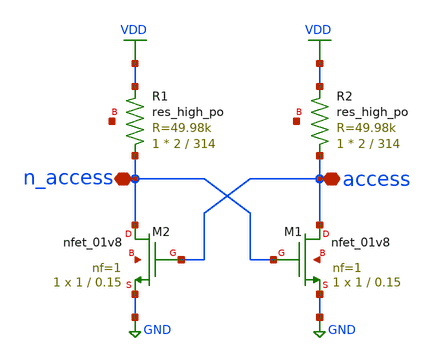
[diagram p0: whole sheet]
** sch_path: analog/schematics/2T2R.sch
**.subckt 2T2R access n_access
*.iopin access
*.iopin n_access
XM1 access n_access GND net1 sky130_fd_pr__nfet_01v8 L=0.15 W=1 nf=1 ad='int((nf+1)/2) * W/nf * 0.29'
+ as='int((nf+2)/2) * W/nf * 0.29' pd='2*int((nf+1)/2) * (W/nf + 0.29)' ps='2*int((nf+2)/2) * (W/nf + 0.29)'
+ nrd='0.29 / W' nrs='0.29 / W' sa=0 sb=0 sd=0 mult=1 m=1
XM2 n_access access GND net2 sky130_fd_pr__nfet_01v8 L=0.15 W=1 nf=1 ad='int((nf+1)/2) * W/nf * 0.29'
+ as='int((nf+2)/2) * W/nf * 0.29' pd='2*int((nf+1)/2) * (W/nf + 0.29)' ps='2*int((nf+2)/2) * (W/nf + 0.29)'
+ nrd='0.29 / W' nrs='0.29 / W' sa=0 sb=0 sd=0 mult=1 m=1
XR1 n_access VDD net3 sky130_fd_pr__res_high_po W=2 L=314 mult=1 m=1
XR2 access VDD net4 sky130_fd_pr__res_high_po W=2 L=314 mult=1 m=1
**.ends
.GLOBAL VDD
.GLOBAL GND
.end
